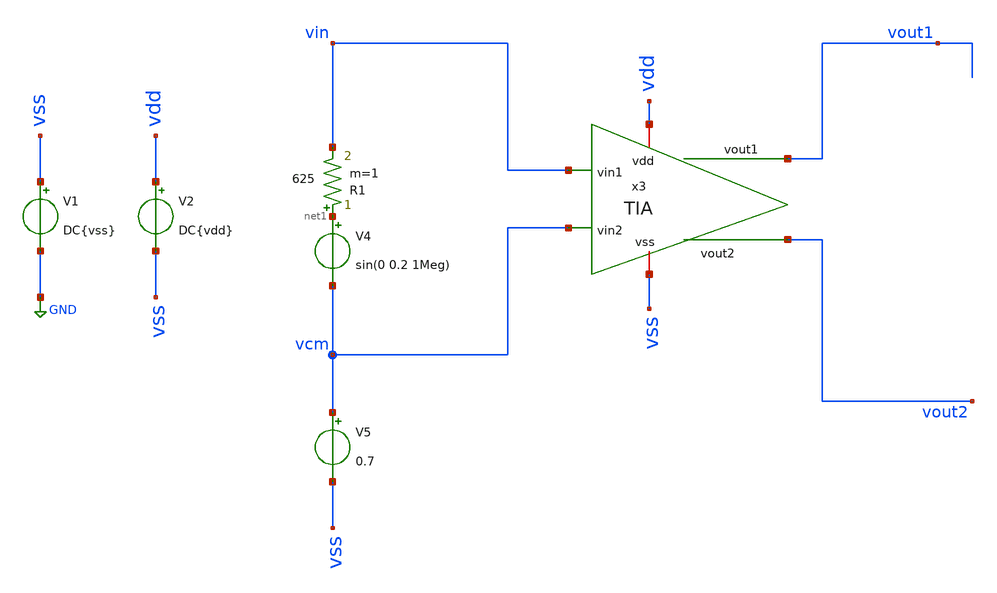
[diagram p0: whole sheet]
** sch_path: sch/tb_TIA.sch
**.subckt tb_TIA
V1 vss GND DC{vss}
V2 vdd vss DC{vdd}
V4 net1 vcm sin(0 0.2 1Meg)
V5 vcm vss 0.7
R1 net1 vin 625 m=1
x3 vout1 vin vdd vss vcm vout2 TIA
**** begin user architecture code




* Circuit Parameters
.param iref = 100u
.param vdd  = 1.8
.param vss  = 0.0
.options TEMP = 65.0

* Include Models
*.lib ~/skywater_pdk/skywater-pdk/libraries/sky130_fd_pr/latest/models/corners/sky130.lib TT

* OP Parameters & Singals to save
.save all

*Simulations
.control

  reset
  tran 0.01u 11u
  setplot tran1
  plot v(vin) v(vcm) v(vout1) v(vout2)
  plot i(v4)

  write tb_tia.raw




.endc

.end



** opencircuitdesign pdks install
.lib $::SKYWATER_MODELS/sky130.lib.spice tt


**** end user architecture code
**.ends
.GLOBAL GND
.end
